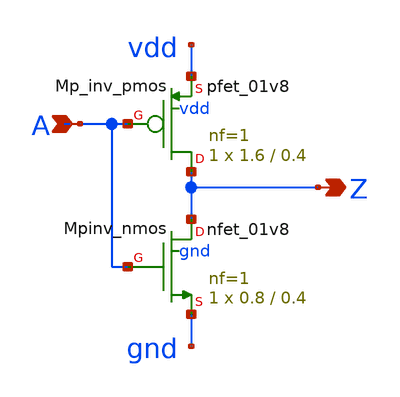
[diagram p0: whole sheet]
** sch_path: sram_2_16_scn4m/pinv_5.sch
**.subckt pinv_5 A Z
*.ipin A
*.opin Z
XMpinv_nmos Z A gnd gnd sky130_fd_pr__nfet_01v8 L=0.4 W=0.8 nf=1 ad='int((nf+1)/2) * W/nf * 0.29' as='int((nf+2)/2) * W/nf * 0.29'
+ pd='2*int((nf+1)/2) * (W/nf + 0.29)' ps='2*int((nf+2)/2) * (W/nf + 0.29)' nrd='0.29 / W' nrs='0.29 / W'
+ sa=0 sb=0 sd=0 mult=1 m=1
XMp_inv_pmos Z A vdd vdd sky130_fd_pr__pfet_01v8 L=0.4 W=1.6 nf=1 ad='int((nf+1)/2) * W/nf * 0.29' as='int((nf+2)/2) * W/nf * 0.29'
+ pd='2*int((nf+1)/2) * (W/nf + 0.29)' ps='2*int((nf+2)/2) * (W/nf + 0.29)' nrd='0.29 / W' nrs='0.29 / W'
+ sa=0 sb=0 sd=0 mult=1 m=1
**.ends
.end
